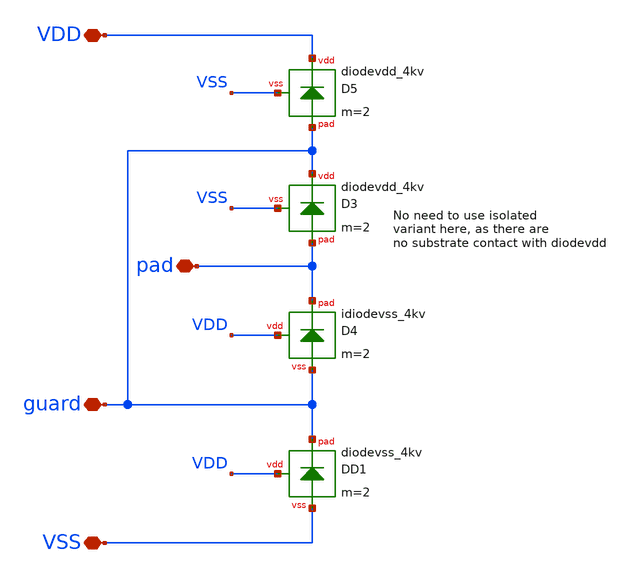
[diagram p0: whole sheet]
** sch_path: trident_test_structures/design_data/xschem/IOPadAnalogGuardLayer/first_stage_diodes_4kv_guard_layer.sch
**.subckt first_stage_diodes_4kv_guard_layer VSS VDD pad guard
*.iopin VSS
*.iopin VDD
*.iopin pad
*.iopin guard
XD5 VDD guard VSS diodevdd_4kv m=2
XD3 guard pad VSS diodevdd_4kv m=2
XD4 VDD pad guard idiodevss_4kv m=2
XD1 VDD guard VSS diodevss_4kv m=2
**.ends
.end
